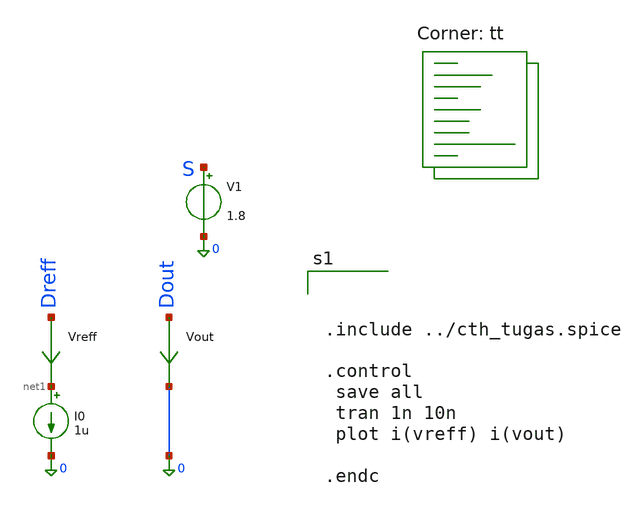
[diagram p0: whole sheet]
** sch_path: Training-3/tb_magic.sch
**.subckt tb_magic
V1 S 0 1.8
Vreff Dreff net1 0
.save i(vreff)
I0 net1 0 1u
Vout Dout 0 0
.save i(vout)
**** begin user architecture code
.lib $::SKYWATER_MODELS/sky130.lib.spice tt



.include ../cth_tugas.spice

.control
 save all
 tran 1n 10n
 plot i(vreff) i(vout)

.endc



**** end user architecture code
**.ends
.end
